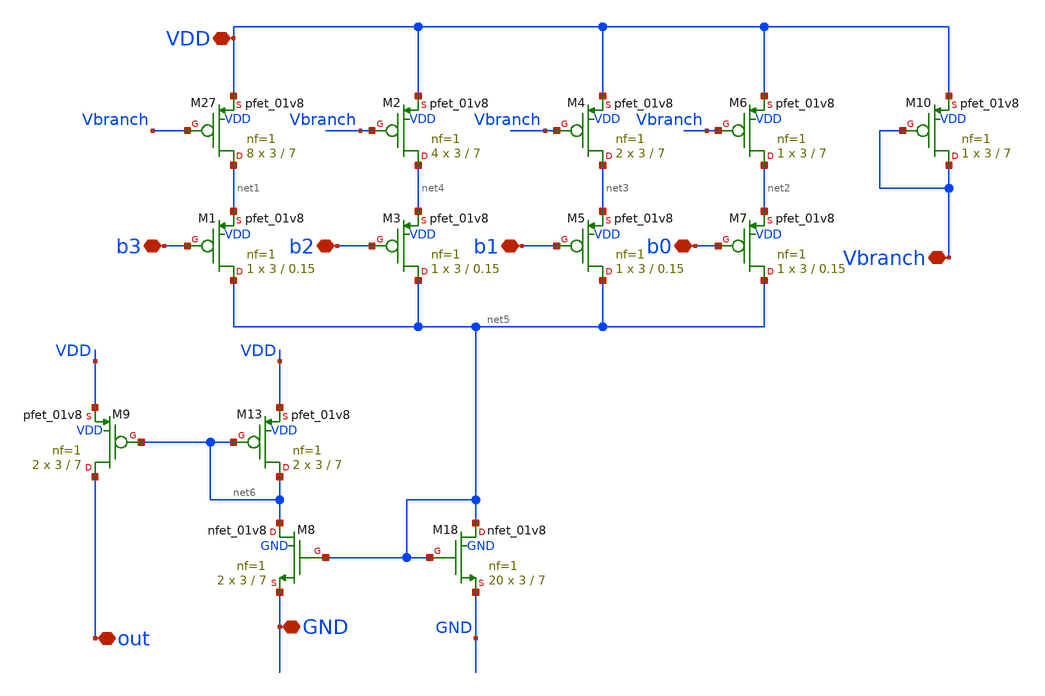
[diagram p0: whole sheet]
** sch_path: xschem/archive/old_blocks/idac_squarer.sch
**.subckt idac_squarer out GND VDD b3 b2 b1 b0 Vbranch
*.iopin out
*.iopin GND
*.iopin VDD
*.iopin b3
*.iopin b2
*.iopin b1
*.iopin b0
*.iopin Vbranch
XM27 net1 Vbranch VDD VDD sky130_fd_pr__pfet_01v8 L=7 W=3 nf=1 ad='int((1 + 1)/2) * 3 / 1 * 0.29' as='int((1 + 2)/2) * 3 / 1 * 0.29'
+ pd='2*int((1 + 1)/2) * (3 / 1 + 0.29)' ps='2*int((1 + 2)/2) * (3 / 1 + 0.29)' nrd='0.29 / 3 ' nrs='0.29 / 3 '
+ sa=0 sb=0 sd=0 mult=8 m=8
XM1 net5 b3 net1 VDD sky130_fd_pr__pfet_01v8 L=0.15 W=3 nf=1 ad='int((1 + 1)/2) * 3 / 1 * 0.29' as='int((1 + 2)/2) * 3 / 1 * 0.29'
+ pd='2*int((1 + 1)/2) * (3 / 1 + 0.29)' ps='2*int((1 + 2)/2) * (3 / 1 + 0.29)' nrd='0.29 / 3 ' nrs='0.29 / 3 '
+ sa=0 sb=0 sd=0 mult=1 m=1
XM2 net4 Vbranch VDD VDD sky130_fd_pr__pfet_01v8 L=7 W=3 nf=1 ad='int((1 + 1)/2) * 3 / 1 * 0.29' as='int((1 + 2)/2) * 3 / 1 * 0.29'
+ pd='2*int((1 + 1)/2) * (3 / 1 + 0.29)' ps='2*int((1 + 2)/2) * (3 / 1 + 0.29)' nrd='0.29 / 3 ' nrs='0.29 / 3 '
+ sa=0 sb=0 sd=0 mult=4 m=4
XM3 net5 b2 net4 VDD sky130_fd_pr__pfet_01v8 L=0.15 W=3 nf=1 ad='int((1 + 1)/2) * 3 / 1 * 0.29' as='int((1 + 2)/2) * 3 / 1 * 0.29'
+ pd='2*int((1 + 1)/2) * (3 / 1 + 0.29)' ps='2*int((1 + 2)/2) * (3 / 1 + 0.29)' nrd='0.29 / 3 ' nrs='0.29 / 3 '
+ sa=0 sb=0 sd=0 mult=1 m=1
XM4 net3 Vbranch VDD VDD sky130_fd_pr__pfet_01v8 L=7 W=3 nf=1 ad='int((1 + 1)/2) * 3 / 1 * 0.29' as='int((1 + 2)/2) * 3 / 1 * 0.29'
+ pd='2*int((1 + 1)/2) * (3 / 1 + 0.29)' ps='2*int((1 + 2)/2) * (3 / 1 + 0.29)' nrd='0.29 / 3 ' nrs='0.29 / 3 '
+ sa=0 sb=0 sd=0 mult=2 m=2
XM5 net5 b1 net3 VDD sky130_fd_pr__pfet_01v8 L=0.15 W=3 nf=1 ad='int((1 + 1)/2) * 3 / 1 * 0.29' as='int((1 + 2)/2) * 3 / 1 * 0.29'
+ pd='2*int((1 + 1)/2) * (3 / 1 + 0.29)' ps='2*int((1 + 2)/2) * (3 / 1 + 0.29)' nrd='0.29 / 3 ' nrs='0.29 / 3 '
+ sa=0 sb=0 sd=0 mult=1 m=1
XM6 net2 Vbranch VDD VDD sky130_fd_pr__pfet_01v8 L=7 W=3 nf=1 ad='int((1 + 1)/2) * 3 / 1 * 0.29' as='int((1 + 2)/2) * 3 / 1 * 0.29'
+ pd='2*int((1 + 1)/2) * (3 / 1 + 0.29)' ps='2*int((1 + 2)/2) * (3 / 1 + 0.29)' nrd='0.29 / 3 ' nrs='0.29 / 3 '
+ sa=0 sb=0 sd=0 mult=1 m=1
XM7 net5 b0 net2 VDD sky130_fd_pr__pfet_01v8 L=0.15 W=3 nf=1 ad='int((1 + 1)/2) * 3 / 1 * 0.29' as='int((1 + 2)/2) * 3 / 1 * 0.29'
+ pd='2*int((1 + 1)/2) * (3 / 1 + 0.29)' ps='2*int((1 + 2)/2) * (3 / 1 + 0.29)' nrd='0.29 / 3 ' nrs='0.29 / 3 '
+ sa=0 sb=0 sd=0 mult=1 m=1
XM18 net5 net5 GND GND sky130_fd_pr__nfet_01v8 L=7 W=3 nf=1 ad='int((nf+1)/2) * W/nf * 0.29' as='int((nf+2)/2) * W/nf * 0.29'
+ pd='2*int((nf+1)/2) * (W/nf + 0.29)' ps='2*int((nf+2)/2) * (W/nf + 0.29)' nrd='0.29 / W' nrs='0.29 / W'
+ sa=0 sb=0 sd=0 mult=20 m=20
XM8 net6 net5 GND GND sky130_fd_pr__nfet_01v8 L=7 W=3 nf=1 ad='int((nf+1)/2) * W/nf * 0.29' as='int((nf+2)/2) * W/nf * 0.29'
+ pd='2*int((nf+1)/2) * (W/nf + 0.29)' ps='2*int((nf+2)/2) * (W/nf + 0.29)' nrd='0.29 / W' nrs='0.29 / W'
+ sa=0 sb=0 sd=0 mult=2 m=2
XM13 net6 net6 VDD VDD sky130_fd_pr__pfet_01v8 L=7 W=3 nf=1 ad='int((1 + 1)/2) * 3 / 1 * 0.29' as='int((1 + 2)/2) * 3 / 1 * 0.29'
+ pd='2*int((1 + 1)/2) * (3 / 1 + 0.29)' ps='2*int((1 + 2)/2) * (3 / 1 + 0.29)' nrd='0.29 / 3 ' nrs='0.29 / 3 '
+ sa=0 sb=0 sd=0 mult=2 m=2
XM9 out net6 VDD VDD sky130_fd_pr__pfet_01v8 L=7 W=3 nf=1 ad='int((1 + 1)/2) * 3 / 1 * 0.29' as='int((1 + 2)/2) * 3 / 1 * 0.29'
+ pd='2*int((1 + 1)/2) * (3 / 1 + 0.29)' ps='2*int((1 + 2)/2) * (3 / 1 + 0.29)' nrd='0.29 / 3 ' nrs='0.29 / 3 '
+ sa=0 sb=0 sd=0 mult=2 m=2
XM10 Vbranch Vbranch VDD VDD sky130_fd_pr__pfet_01v8 L=7 W=3 nf=1 ad='int((1 + 1)/2) * 3 / 1 * 0.29'
+ as='int((1 + 2)/2) * 3 / 1 * 0.29' pd='2*int((1 + 1)/2) * (3 / 1 + 0.29)' ps='2*int((1 + 2)/2) * (3 / 1 + 0.29)'
+ nrd='0.29 / 3 ' nrs='0.29 / 3 ' sa=0 sb=0 sd=0 mult=1 m=1
**.ends
.end
